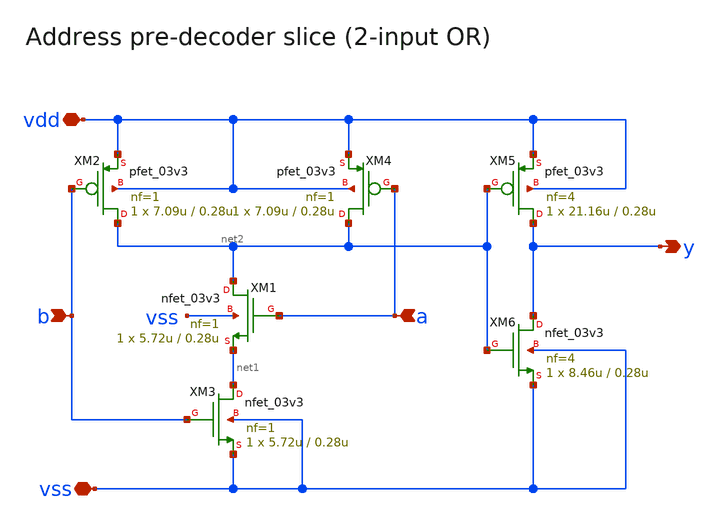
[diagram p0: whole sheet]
** sch_path: cells/gf180mcu_ocd_ip_sram__sram256x8m8wm1/xschem/xpredec0_xa_3v256x8m81.sch
**.subckt xpredec0_xa_3v256x8m81 vdd vss a b y
*.iopin vdd
*.iopin vss
*.ipin a
*.ipin b
*.opin y
XM1 net2 a net1 vss nfet_03v3 L=0.28u W=5.72u nf=1 ad='int((nf+1)/2) * W/nf * 0.18u' as='int((nf+2)/2) * W/nf * 0.18u'
+ pd='2*int((nf+1)/2) * (W/nf + 0.18u)' ps='2*int((nf+2)/2) * (W/nf + 0.18u)' nrd='0.18u / W' nrs='0.18u / W'
+ sa=0 sb=0 sd=0 m=1
XM2 net2 b vdd vdd pfet_03v3 L=0.28u W=7.09u nf=1 ad='int((nf+1)/2) * W/nf * 0.18u' as='int((nf+2)/2) * W/nf * 0.18u'
+ pd='2*int((nf+1)/2) * (W/nf + 0.18u)' ps='2*int((nf+2)/2) * (W/nf + 0.18u)' nrd='0.18u / W' nrs='0.18u / W'
+ sa=0 sb=0 sd=0 m=1
XM3 net1 b vss vss nfet_03v3 L=0.28u W=5.72u nf=1 ad='int((nf+1)/2) * W/nf * 0.18u' as='int((nf+2)/2) * W/nf * 0.18u'
+ pd='2*int((nf+1)/2) * (W/nf + 0.18u)' ps='2*int((nf+2)/2) * (W/nf + 0.18u)' nrd='0.18u / W' nrs='0.18u / W'
+ sa=0 sb=0 sd=0 m=1
XM4 net2 a vdd vdd pfet_03v3 L=0.28u W=7.09u nf=1 ad='int((nf+1)/2) * W/nf * 0.18u' as='int((nf+2)/2) * W/nf * 0.18u'
+ pd='2*int((nf+1)/2) * (W/nf + 0.18u)' ps='2*int((nf+2)/2) * (W/nf + 0.18u)' nrd='0.18u / W' nrs='0.18u / W'
+ sa=0 sb=0 sd=0 m=1
XM5 y net2 vdd vdd pfet_03v3 L=0.28u W=21.16u nf=4 ad='int((nf+1)/2) * W/nf * 0.18u' as='int((nf+2)/2) * W/nf * 0.18u'
+ pd='2*int((nf+1)/2) * (W/nf + 0.18u)' ps='2*int((nf+2)/2) * (W/nf + 0.18u)' nrd='0.18u / W' nrs='0.18u / W'
+ sa=0 sb=0 sd=0 m=1
XM6 y net2 vss vss nfet_03v3 L=0.28u W=8.46u nf=4 ad='int((nf+1)/2) * W/nf * 0.18u' as='int((nf+2)/2) * W/nf * 0.18u'
+ pd='2*int((nf+1)/2) * (W/nf + 0.18u)' ps='2*int((nf+2)/2) * (W/nf + 0.18u)' nrd='0.18u / W' nrs='0.18u / W'
+ sa=0 sb=0 sd=0 m=1
**.ends
.end
